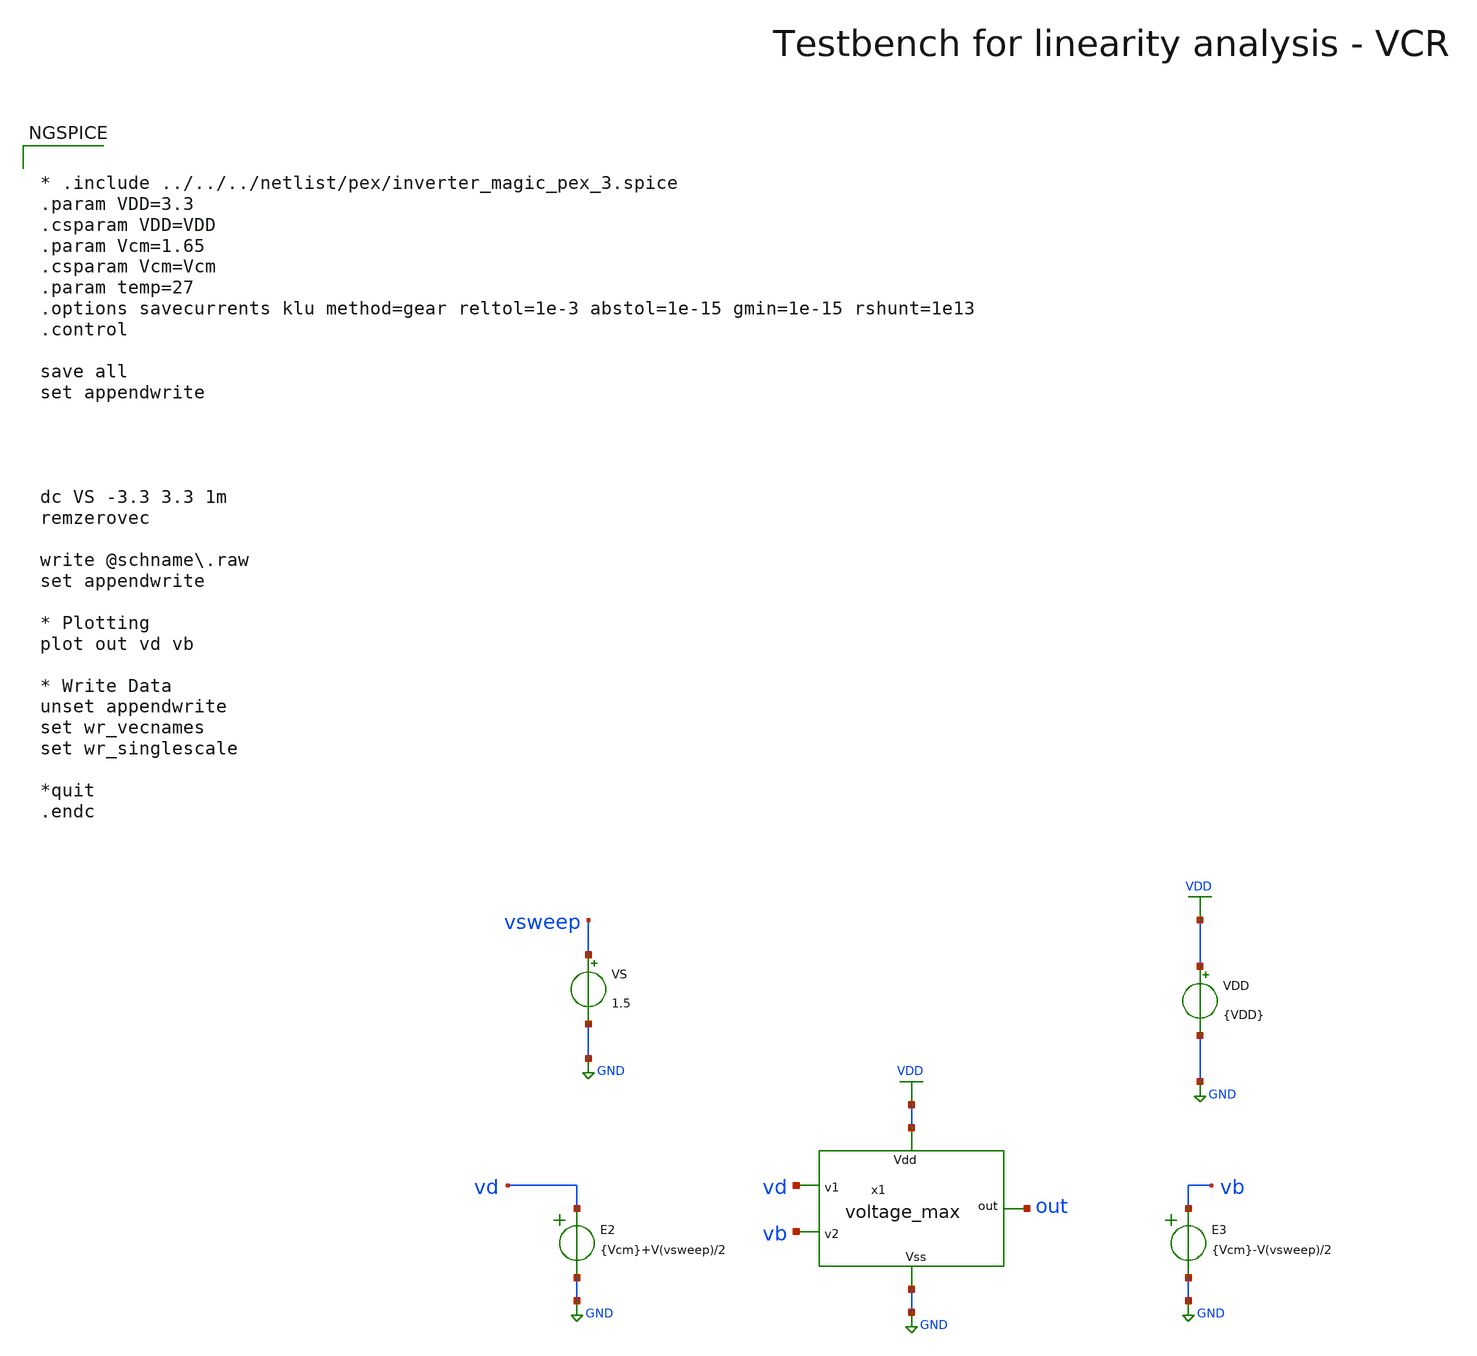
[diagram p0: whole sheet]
** sch_path: macros/heichips26_vcr/macros/vcr_bisection/testbenches/xschem/vmax_tb.sch
**.subckt vmax_tb
VDD VDD GND {VDD}
VS vsweep GND 1.5
E2 vd GND VOL=' {Vcm}+V(vsweep)/2 '
E3 vb GND VOL=' {Vcm}-V(vsweep)/2 '
x1 vd VDD GND out vb voltage_max
**** begin user architecture code

.lib cornerMOSlv.lib mos_tt
.lib cornerMOShv.lib mos_tt
.lib cornerRES.lib res_typ
.lib cornerDIO.lib dio_tt
.lib cornerCAP.lib cap_typ



* .include ../../../netlist/pex/inverter_magic_pex_3.spice
.param VDD=3.3
.csparam VDD=VDD
.param Vcm=1.65
.csparam Vcm=Vcm
.param temp=27
.options savecurrents klu method=gear reltol=1e-3 abstol=1e-15 gmin=1e-15 rshunt=1e13
.control

save all
set appendwrite




dc VS -3.3 3.3 1m
remzerovec

write @schname\.raw
set appendwrite

* Plotting
plot out vd vb

* Write Data
unset appendwrite
set wr_vecnames
set wr_singlescale

*quit
.endc


**** end user architecture code
**.ends
.GLOBAL GND
.GLOBAL VDD
.end
